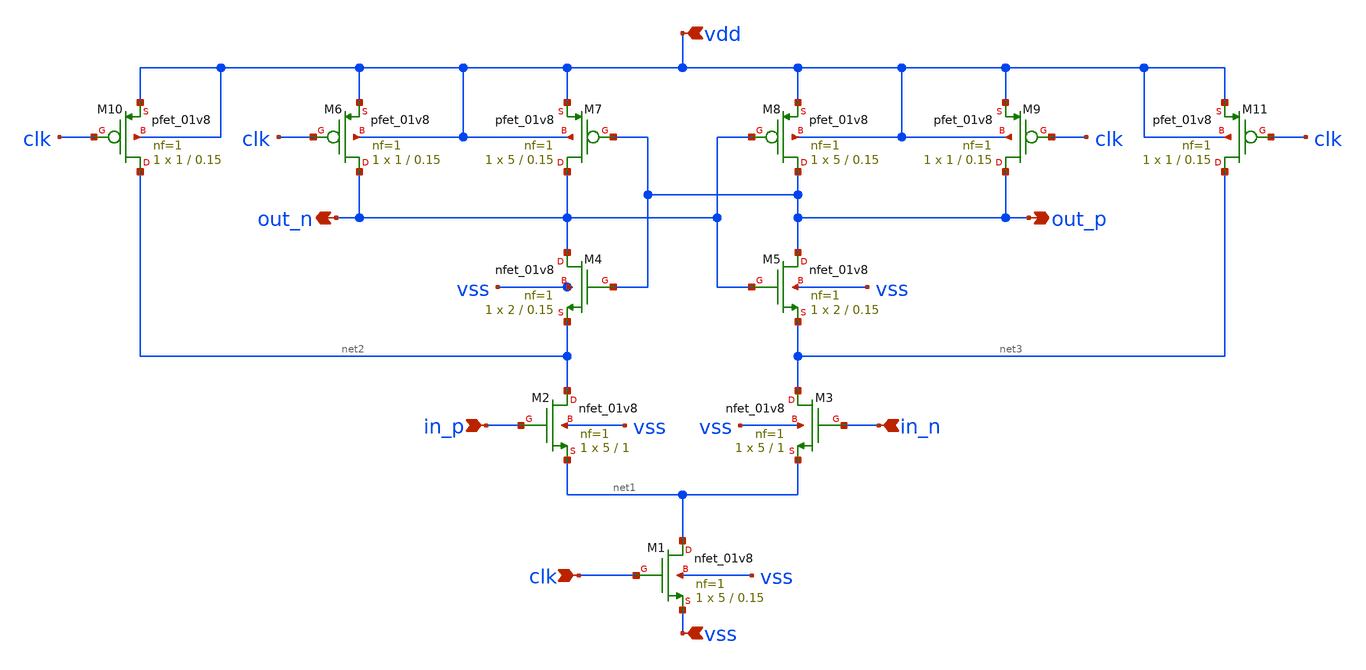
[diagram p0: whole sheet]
** sch_path: sch/clk_comp.sch
**.subckt clk_comp in_p in_n vss vdd clk out_p out_n
*.ipin in_p
*.ipin in_n
*.ipin vss
*.ipin vdd
*.ipin clk
*.opin out_p
*.opin out_n
XM1 net1 clk vss vss sky130_fd_pr__nfet_01v8 L=0.15 W=5 nf=1 ad='int((nf+1)/2) * W/nf * 0.29' as='int((nf+2)/2) * W/nf * 0.29'
+ pd='2*int((nf+1)/2) * (W/nf + 0.29)' ps='2*int((nf+2)/2) * (W/nf + 0.29)' nrd='0.29 / W' nrs='0.29 / W'
+ sa=0 sb=0 sd=0 mult=1 m=1
XM2 net2 in_p net1 vss sky130_fd_pr__nfet_01v8 L=1 W=5 nf=1 ad='int((nf+1)/2) * W/nf * 0.29' as='int((nf+2)/2) * W/nf * 0.29'
+ pd='2*int((nf+1)/2) * (W/nf + 0.29)' ps='2*int((nf+2)/2) * (W/nf + 0.29)' nrd='0.29 / W' nrs='0.29 / W'
+ sa=0 sb=0 sd=0 mult=1 m=1
XM3 net3 in_n net1 vss sky130_fd_pr__nfet_01v8 L=1 W=5 nf=1 ad='int((nf+1)/2) * W/nf * 0.29' as='int((nf+2)/2) * W/nf * 0.29'
+ pd='2*int((nf+1)/2) * (W/nf + 0.29)' ps='2*int((nf+2)/2) * (W/nf + 0.29)' nrd='0.29 / W' nrs='0.29 / W'
+ sa=0 sb=0 sd=0 mult=1 m=1
XM4 out_n out_p net2 vss sky130_fd_pr__nfet_01v8 L=0.15 W=2 nf=1 ad='int((nf+1)/2) * W/nf * 0.29' as='int((nf+2)/2) * W/nf * 0.29'
+ pd='2*int((nf+1)/2) * (W/nf + 0.29)' ps='2*int((nf+2)/2) * (W/nf + 0.29)' nrd='0.29 / W' nrs='0.29 / W'
+ sa=0 sb=0 sd=0 mult=1 m=1
XM5 out_p out_n net3 vss sky130_fd_pr__nfet_01v8 L=0.15 W=2 nf=1 ad='int((nf+1)/2) * W/nf * 0.29' as='int((nf+2)/2) * W/nf * 0.29'
+ pd='2*int((nf+1)/2) * (W/nf + 0.29)' ps='2*int((nf+2)/2) * (W/nf + 0.29)' nrd='0.29 / W' nrs='0.29 / W'
+ sa=0 sb=0 sd=0 mult=1 m=1
XM6 out_n clk vdd vdd sky130_fd_pr__pfet_01v8 L=0.15 W=1 nf=1 ad='int((nf+1)/2) * W/nf * 0.29' as='int((nf+2)/2) * W/nf * 0.29'
+ pd='2*int((nf+1)/2) * (W/nf + 0.29)' ps='2*int((nf+2)/2) * (W/nf + 0.29)' nrd='0.29 / W' nrs='0.29 / W'
+ sa=0 sb=0 sd=0 mult=1 m=1
XM7 out_n out_p vdd vdd sky130_fd_pr__pfet_01v8 L=0.15 W=5 nf=1 ad='int((nf+1)/2) * W/nf * 0.29' as='int((nf+2)/2) * W/nf * 0.29'
+ pd='2*int((nf+1)/2) * (W/nf + 0.29)' ps='2*int((nf+2)/2) * (W/nf + 0.29)' nrd='0.29 / W' nrs='0.29 / W'
+ sa=0 sb=0 sd=0 mult=1 m=1
XM8 out_p out_n vdd vdd sky130_fd_pr__pfet_01v8 L=0.15 W=5 nf=1 ad='int((nf+1)/2) * W/nf * 0.29' as='int((nf+2)/2) * W/nf * 0.29'
+ pd='2*int((nf+1)/2) * (W/nf + 0.29)' ps='2*int((nf+2)/2) * (W/nf + 0.29)' nrd='0.29 / W' nrs='0.29 / W'
+ sa=0 sb=0 sd=0 mult=1 m=1
XM9 out_p clk vdd vdd sky130_fd_pr__pfet_01v8 L=0.15 W=1 nf=1 ad='int((nf+1)/2) * W/nf * 0.29' as='int((nf+2)/2) * W/nf * 0.29'
+ pd='2*int((nf+1)/2) * (W/nf + 0.29)' ps='2*int((nf+2)/2) * (W/nf + 0.29)' nrd='0.29 / W' nrs='0.29 / W'
+ sa=0 sb=0 sd=0 mult=1 m=1
XM10 net2 clk vdd vdd sky130_fd_pr__pfet_01v8 L=0.15 W=1 nf=1 ad='int((nf+1)/2) * W/nf * 0.29' as='int((nf+2)/2) * W/nf * 0.29'
+ pd='2*int((nf+1)/2) * (W/nf + 0.29)' ps='2*int((nf+2)/2) * (W/nf + 0.29)' nrd='0.29 / W' nrs='0.29 / W'
+ sa=0 sb=0 sd=0 mult=1 m=1
XM11 net3 clk vdd vdd sky130_fd_pr__pfet_01v8 L=0.15 W=1 nf=1 ad='int((nf+1)/2) * W/nf * 0.29' as='int((nf+2)/2) * W/nf * 0.29'
+ pd='2*int((nf+1)/2) * (W/nf + 0.29)' ps='2*int((nf+2)/2) * (W/nf + 0.29)' nrd='0.29 / W' nrs='0.29 / W'
+ sa=0 sb=0 sd=0 mult=1 m=1
**.ends
.end
